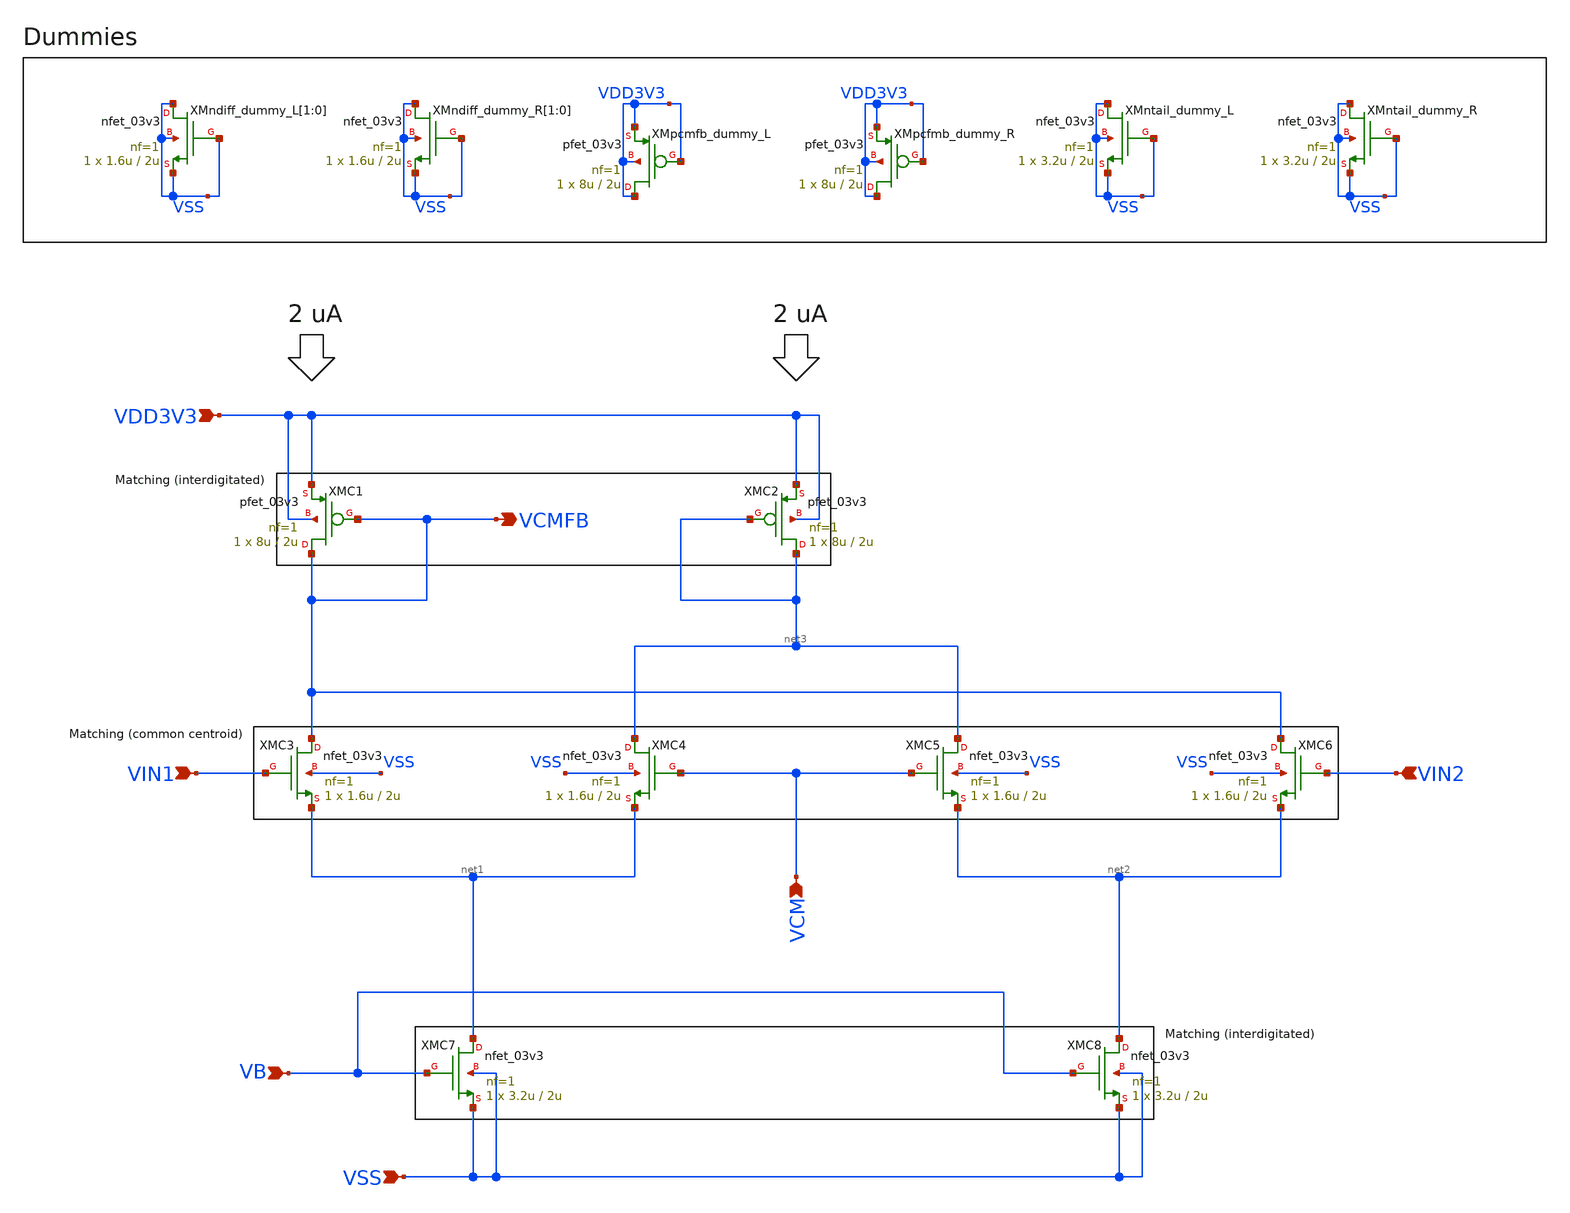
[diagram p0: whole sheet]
** sch_path: designs/libs/core_ina/ina_cmfb/ina_cmfb.sch
**.subckt ina_cmfb VIN1 VIN2 VCMFB VCM VSS VB VDD3V3
*.ipin VIN1
*.ipin VIN2
*.opin VCMFB
*.ipin VCM
*.ipin VSS
*.ipin VB
*.ipin VDD3V3
XMC1 VCMFB VCMFB VDD3V3 VDD3V3 pfet_03v3 L=2u W=8u nf=1 ad='int((nf+1)/2) * W/nf * 0.18u' as='int((nf+2)/2) * W/nf * 0.18u'
+ pd='2*int((nf+1)/2) * (W/nf + 0.18u)' ps='2*int((nf+2)/2) * (W/nf + 0.18u)' nrd='0.18u / W' nrs='0.18u / W'
+ sa=0 sb=0 sd=0 m=1
XMC3 VCMFB VIN1 net1 VSS nfet_03v3 L=2u W=1.6u nf=1 ad='int((nf+1)/2) * W/nf * 0.18u' as='int((nf+2)/2) * W/nf * 0.18u'
+ pd='2*int((nf+1)/2) * (W/nf + 0.18u)' ps='2*int((nf+2)/2) * (W/nf + 0.18u)' nrd='0.18u / W' nrs='0.18u / W'
+ sa=0 sb=0 sd=0 m=1
XMC4 net3 VCM net1 VSS nfet_03v3 L=2u W=1.6u nf=1 ad='int((nf+1)/2) * W/nf * 0.18u' as='int((nf+2)/2) * W/nf * 0.18u'
+ pd='2*int((nf+1)/2) * (W/nf + 0.18u)' ps='2*int((nf+2)/2) * (W/nf + 0.18u)' nrd='0.18u / W' nrs='0.18u / W'
+ sa=0 sb=0 sd=0 m=1
XMC7 net1 VB VSS VSS nfet_03v3 L=2u W=3.2u nf=1 ad='int((nf+1)/2) * W/nf * 0.18u' as='int((nf+2)/2) * W/nf * 0.18u'
+ pd='2*int((nf+1)/2) * (W/nf + 0.18u)' ps='2*int((nf+2)/2) * (W/nf + 0.18u)' nrd='0.18u / W' nrs='0.18u / W'
+ sa=0 sb=0 sd=0 m=1
XMC5 net3 VCM net2 VSS nfet_03v3 L=2u W=1.6u nf=1 ad='int((nf+1)/2) * W/nf * 0.18u' as='int((nf+2)/2) * W/nf * 0.18u'
+ pd='2*int((nf+1)/2) * (W/nf + 0.18u)' ps='2*int((nf+2)/2) * (W/nf + 0.18u)' nrd='0.18u / W' nrs='0.18u / W'
+ sa=0 sb=0 sd=0 m=1
XMC6 VCMFB VIN2 net2 VSS nfet_03v3 L=2u W=1.6u nf=1 ad='int((nf+1)/2) * W/nf * 0.18u' as='int((nf+2)/2) * W/nf * 0.18u'
+ pd='2*int((nf+1)/2) * (W/nf + 0.18u)' ps='2*int((nf+2)/2) * (W/nf + 0.18u)' nrd='0.18u / W' nrs='0.18u / W'
+ sa=0 sb=0 sd=0 m=1
XMC8 net2 VB VSS VSS nfet_03v3 L=2u W=3.2u nf=1 ad='int((nf+1)/2) * W/nf * 0.18u' as='int((nf+2)/2) * W/nf * 0.18u'
+ pd='2*int((nf+1)/2) * (W/nf + 0.18u)' ps='2*int((nf+2)/2) * (W/nf + 0.18u)' nrd='0.18u / W' nrs='0.18u / W'
+ sa=0 sb=0 sd=0 m=1
XMC2 net3 net3 VDD3V3 VDD3V3 pfet_03v3 L=2u W=8u nf=1 ad='int((nf+1)/2) * W/nf * 0.18u' as='int((nf+2)/2) * W/nf * 0.18u'
+ pd='2*int((nf+1)/2) * (W/nf + 0.18u)' ps='2*int((nf+2)/2) * (W/nf + 0.18u)' nrd='0.18u / W' nrs='0.18u / W'
+ sa=0 sb=0 sd=0 m=1
XMndiff_dummy_L[1] VSS VSS VSS VSS nfet_03v3 L=2u W=1.6u nf=1 ad='int((nf+1)/2) * W/nf * 0.18u' as='int((nf+2)/2) * W/nf * 0.18u'
+ pd='2*int((nf+1)/2) * (W/nf + 0.18u)' ps='2*int((nf+2)/2) * (W/nf + 0.18u)' nrd='0.18u / W' nrs='0.18u / W'
+ sa=0 sb=0 sd=0 m=1
XMndiff_dummy_L[0] VSS VSS VSS VSS nfet_03v3 L=2u W=1.6u nf=1 ad='int((nf+1)/2) * W/nf * 0.18u' as='int((nf+2)/2) * W/nf * 0.18u'
+ pd='2*int((nf+1)/2) * (W/nf + 0.18u)' ps='2*int((nf+2)/2) * (W/nf + 0.18u)' nrd='0.18u / W' nrs='0.18u / W'
+ sa=0 sb=0 sd=0 m=1
XMndiff_dummy_R[1] VSS VSS VSS VSS nfet_03v3 L=2u W=1.6u nf=1 ad='int((nf+1)/2) * W/nf * 0.18u' as='int((nf+2)/2) * W/nf * 0.18u'
+ pd='2*int((nf+1)/2) * (W/nf + 0.18u)' ps='2*int((nf+2)/2) * (W/nf + 0.18u)' nrd='0.18u / W' nrs='0.18u / W'
+ sa=0 sb=0 sd=0 m=1
XMndiff_dummy_R[0] VSS VSS VSS VSS nfet_03v3 L=2u W=1.6u nf=1 ad='int((nf+1)/2) * W/nf * 0.18u' as='int((nf+2)/2) * W/nf * 0.18u'
+ pd='2*int((nf+1)/2) * (W/nf + 0.18u)' ps='2*int((nf+2)/2) * (W/nf + 0.18u)' nrd='0.18u / W' nrs='0.18u / W'
+ sa=0 sb=0 sd=0 m=1
XMpcmfb_dummy_L VDD3V3 VDD3V3 VDD3V3 VDD3V3 pfet_03v3 L=2u W=8u nf=1 ad='int((nf+1)/2) * W/nf * 0.18u'
+ as='int((nf+2)/2) * W/nf * 0.18u' pd='2*int((nf+1)/2) * (W/nf + 0.18u)' ps='2*int((nf+2)/2) * (W/nf + 0.18u)'
+ nrd='0.18u / W' nrs='0.18u / W' sa=0 sb=0 sd=0 m=1
XMpcfmb_dummy_R VDD3V3 VDD3V3 VDD3V3 VDD3V3 pfet_03v3 L=2u W=8u nf=1 ad='int((nf+1)/2) * W/nf * 0.18u'
+ as='int((nf+2)/2) * W/nf * 0.18u' pd='2*int((nf+1)/2) * (W/nf + 0.18u)' ps='2*int((nf+2)/2) * (W/nf + 0.18u)'
+ nrd='0.18u / W' nrs='0.18u / W' sa=0 sb=0 sd=0 m=1
XMntail_dummy_L VSS VSS VSS VSS nfet_03v3 L=2u W=3.2u nf=1 ad='int((nf+1)/2) * W/nf * 0.18u' as='int((nf+2)/2) * W/nf * 0.18u'
+ pd='2*int((nf+1)/2) * (W/nf + 0.18u)' ps='2*int((nf+2)/2) * (W/nf + 0.18u)' nrd='0.18u / W' nrs='0.18u / W'
+ sa=0 sb=0 sd=0 m=1
XMntail_dummy_R VSS VSS VSS VSS nfet_03v3 L=2u W=3.2u nf=1 ad='int((nf+1)/2) * W/nf * 0.18u' as='int((nf+2)/2) * W/nf * 0.18u'
+ pd='2*int((nf+1)/2) * (W/nf + 0.18u)' ps='2*int((nf+2)/2) * (W/nf + 0.18u)' nrd='0.18u / W' nrs='0.18u / W'
+ sa=0 sb=0 sd=0 m=1
**.ends
.end
